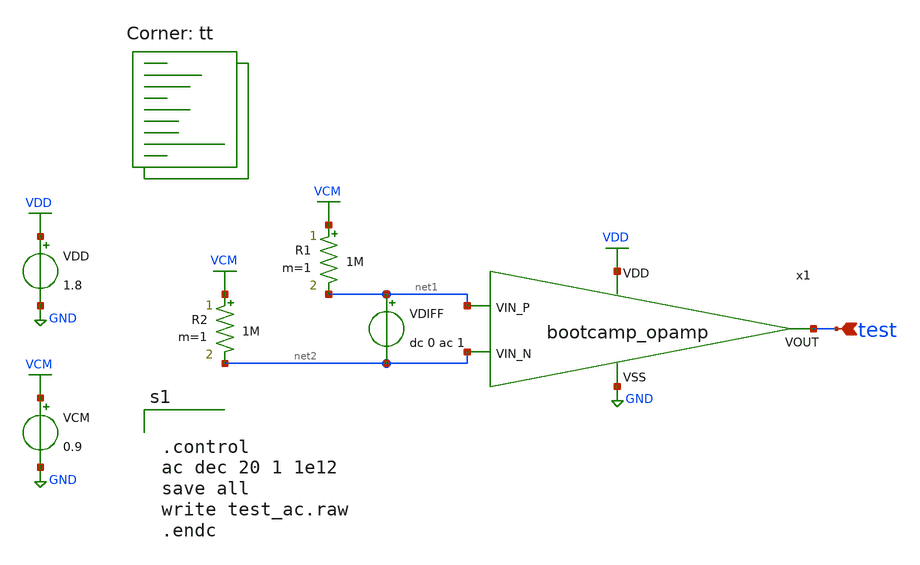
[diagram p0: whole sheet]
** sch_path: analog/schematics/tb_ac_analysis.sch
**.subckt tb_ac_analysis test
*.ipin test
x1 VDD test net2 net1 GND bootcamp_opamp
R1 VCM net1 1M m=1
R2 VCM net2 1M m=1
VDD VDD GND 1.8
VCM VCM GND 0.9
VDIFF net1 net2 dc 0 ac 1
**** begin user architecture code


.control
ac dec 20 1 1e12
save all
write test_ac.raw
.endc


.lib $::SKYWATER_MODELS/sky130.lib.spice tt
**** end user architecture code
**.ends

* expanding   symbol:  bootcamp_opamp.sym # of pins=5
** sym_path: analog/schematics/bootcamp_opamp.sym
** sch_path: analog/schematics/bootcamp_opamp.sch
.subckt bootcamp_opamp VDD VOUT VIN_N VIN_P VSS
*.ipin VIN_P
*.ipin VIN_N
*.ipin VDD
*.ipin VSS
*.opin VOUT
XM1 net1 VIN_P net3 VSS sky130_fd_pr__nfet_01v8 L=0.5 W=16 nf=1 ad='int((nf+1)/2) * W/nf * 0.29' as='int((nf+2)/2) * W/nf * 0.29'
+ pd='2*int((nf+1)/2) * (W/nf + 0.29)' ps='2*int((nf+2)/2) * (W/nf + 0.29)' nrd='0.29 / W' nrs='0.29 / W'
+ sa=0 sb=0 sd=0 mult=1 m=1
XM2 net2 VIN_N net3 VSS sky130_fd_pr__nfet_01v8 L=0.5 W=16 nf=1 ad='int((nf+1)/2) * W/nf * 0.29' as='int((nf+2)/2) * W/nf * 0.29'
+ pd='2*int((nf+1)/2) * (W/nf + 0.29)' ps='2*int((nf+2)/2) * (W/nf + 0.29)' nrd='0.29 / W' nrs='0.29 / W'
+ sa=0 sb=0 sd=0 mult=1 m=1
XM3 net1 net1 VDD VDD sky130_fd_pr__pfet_01v8 L=0.5 W=10 nf=1 ad='int((nf+1)/2) * W/nf * 0.29' as='int((nf+2)/2) * W/nf * 0.29'
+ pd='2*int((nf+1)/2) * (W/nf + 0.29)' ps='2*int((nf+2)/2) * (W/nf + 0.29)' nrd='0.29 / W' nrs='0.29 / W'
+ sa=0 sb=0 sd=0 mult=1 m=1
XM4 net2 net1 VDD VDD sky130_fd_pr__pfet_01v8 L=0.5 W=10 nf=1 ad='int((nf+1)/2) * W/nf * 0.29' as='int((nf+2)/2) * W/nf * 0.29'
+ pd='2*int((nf+1)/2) * (W/nf + 0.29)' ps='2*int((nf+2)/2) * (W/nf + 0.29)' nrd='0.29 / W' nrs='0.29 / W'
+ sa=0 sb=0 sd=0 mult=1 m=1
XM5 net3 VDD VSS VSS sky130_fd_pr__nfet_01v8 L=2 W=4 nf=1 ad='int((nf+1)/2) * W/nf * 0.29' as='int((nf+2)/2) * W/nf * 0.29'
+ pd='2*int((nf+1)/2) * (W/nf + 0.29)' ps='2*int((nf+2)/2) * (W/nf + 0.29)' nrd='0.29 / W' nrs='0.29 / W'
+ sa=0 sb=0 sd=0 mult=1 m=1
XM6 VOUT net2 VDD VDD sky130_fd_pr__pfet_01v8 L=0.5 W=10 nf=1 ad='int((nf+1)/2) * W/nf * 0.29' as='int((nf+2)/2) * W/nf * 0.29'
+ pd='2*int((nf+1)/2) * (W/nf + 0.29)' ps='2*int((nf+2)/2) * (W/nf + 0.29)' nrd='0.29 / W' nrs='0.29 / W'
+ sa=0 sb=0 sd=0 mult=1 m=1
XM7 VOUT VDD VSS VSS sky130_fd_pr__nfet_01v8 L=2 W=4 nf=1 ad='int((nf+1)/2) * W/nf * 0.29' as='int((nf+2)/2) * W/nf * 0.29'
+ pd='2*int((nf+1)/2) * (W/nf + 0.29)' ps='2*int((nf+2)/2) * (W/nf + 0.29)' nrd='0.29 / W' nrs='0.29 / W'
+ sa=0 sb=0 sd=0 mult=1 m=1
XM8 VDD VDD VSS VSS sky130_fd_pr__nfet_01v8 L=0.8 W=4 nf=1 ad='int((nf+1)/2) * W/nf * 0.29' as='int((nf+2)/2) * W/nf * 0.29'
+ pd='2*int((nf+1)/2) * (W/nf + 0.29)' ps='2*int((nf+2)/2) * (W/nf + 0.29)' nrd='0.29 / W' nrs='0.29 / W'
+ sa=0 sb=0 sd=0 mult=1 m=1
XC1 net2 VOUT sky130_fd_pr__cap_mim_m3_1 W=50 L=10 MF=1 m=1
.ends

.GLOBAL GND
.GLOBAL VDD
.GLOBAL VCM
.end
